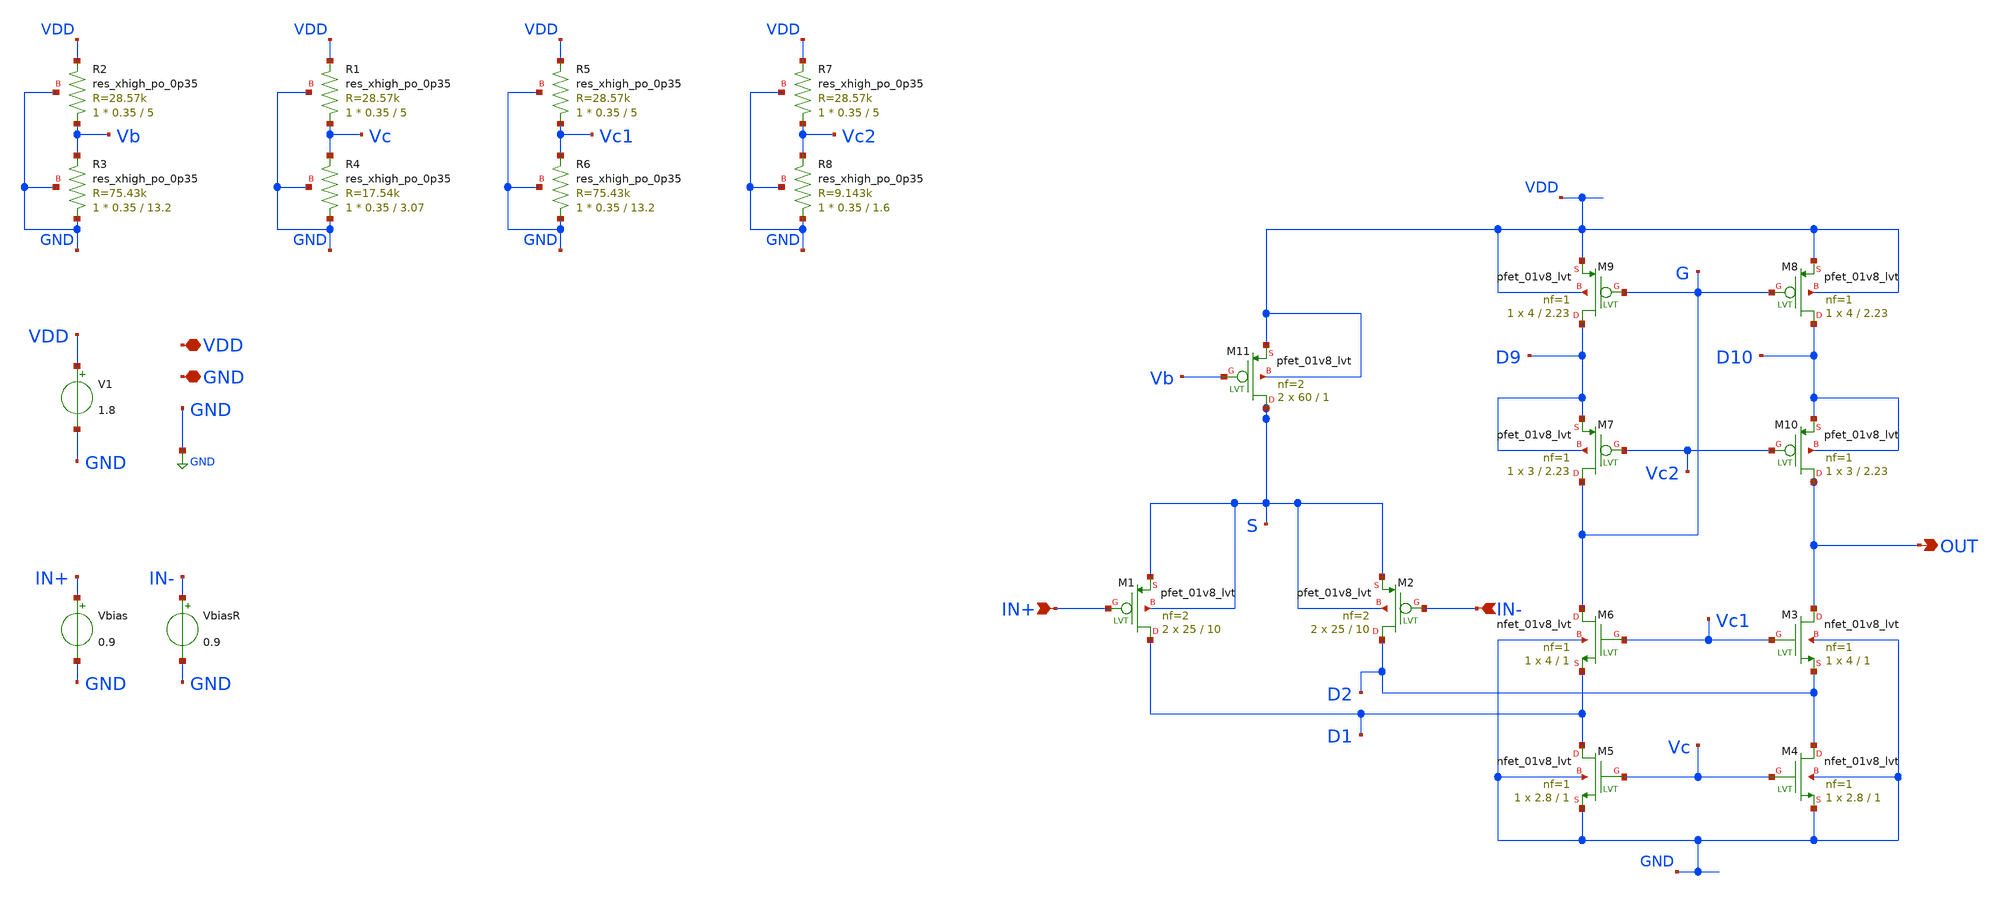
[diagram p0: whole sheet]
** sch_path: xschem/OTA_FoldedCascode1_MC.sch
**.subckt OTA_FoldedCascode1_MC VDD GND IN+ IN- OUT
*.iopin VDD
*.iopin GND
*.ipin IN+
*.ipin IN-
*.opin OUT
V1 VDD GND 1.8
Vbias IN+ GND 0.9
VbiasR IN- GND 0.9
XM11 S Vb VDD VDD sky130_fd_pr__pfet_01v8_lvt L=1 W=60 nf=2 ad='int((nf+1)/2) * W/nf * 0.29' as='int((nf+2)/2) * W/nf * 0.29'
+ pd='2*int((nf+1)/2) * (W/nf + 0.29)' ps='2*int((nf+2)/2) * (W/nf + 0.29)' nrd='0.29 / W' nrs='0.29 / W'
+ sa=0 sb=0 sd=0 mult=2 m=2
XM1 D1 IN+ S S sky130_fd_pr__pfet_01v8_lvt L=10 W=25 nf=2 ad='int((nf+1)/2) * W/nf * 0.29' as='int((nf+2)/2) * W/nf * 0.29'
+ pd='2*int((nf+1)/2) * (W/nf + 0.29)' ps='2*int((nf+2)/2) * (W/nf + 0.29)' nrd='0.29 / W' nrs='0.29 / W'
+ sa=0 sb=0 sd=0 mult=2 m=2
XM2 D2 IN- S S sky130_fd_pr__pfet_01v8_lvt L=10 W=25 nf=2 ad='int((nf+1)/2) * W/nf * 0.29' as='int((nf+2)/2) * W/nf * 0.29'
+ pd='2*int((nf+1)/2) * (W/nf + 0.29)' ps='2*int((nf+2)/2) * (W/nf + 0.29)' nrd='0.29 / W' nrs='0.29 / W'
+ sa=0 sb=0 sd=0 mult=2 m=2
XM3 OUT Vc1 D2 GND sky130_fd_pr__nfet_01v8_lvt L=1 W=4 nf=1 ad='int((nf+1)/2) * W/nf * 0.29' as='int((nf+2)/2) * W/nf * 0.29'
+ pd='2*int((nf+1)/2) * (W/nf + 0.29)' ps='2*int((nf+2)/2) * (W/nf + 0.29)' nrd='0.29 / W' nrs='0.29 / W'
+ sa=0 sb=0 sd=0 mult=1 m=1
XM4 D2 Vc GND GND sky130_fd_pr__nfet_01v8_lvt L=1 W=2.8 nf=1 ad='int((nf+1)/2) * W/nf * 0.29' as='int((nf+2)/2) * W/nf * 0.29'
+ pd='2*int((nf+1)/2) * (W/nf + 0.29)' ps='2*int((nf+2)/2) * (W/nf + 0.29)' nrd='0.29 / W' nrs='0.29 / W'
+ sa=0 sb=0 sd=0 mult=1 m=1
XM5 D1 Vc GND GND sky130_fd_pr__nfet_01v8_lvt L=1 W=2.8 nf=1 ad='int((nf+1)/2) * W/nf * 0.29' as='int((nf+2)/2) * W/nf * 0.29'
+ pd='2*int((nf+1)/2) * (W/nf + 0.29)' ps='2*int((nf+2)/2) * (W/nf + 0.29)' nrd='0.29 / W' nrs='0.29 / W'
+ sa=0 sb=0 sd=0 mult=1 m=1
XM6 G Vc1 D1 GND sky130_fd_pr__nfet_01v8_lvt L=1 W=4 nf=1 ad='int((nf+1)/2) * W/nf * 0.29' as='int((nf+2)/2) * W/nf * 0.29'
+ pd='2*int((nf+1)/2) * (W/nf + 0.29)' ps='2*int((nf+2)/2) * (W/nf + 0.29)' nrd='0.29 / W' nrs='0.29 / W'
+ sa=0 sb=0 sd=0 mult=1 m=1
XM7 G Vc2 D9 D9 sky130_fd_pr__pfet_01v8_lvt L=2.23 W=3 nf=1 ad='int((nf+1)/2) * W/nf * 0.29' as='int((nf+2)/2) * W/nf * 0.29'
+ pd='2*int((nf+1)/2) * (W/nf + 0.29)' ps='2*int((nf+2)/2) * (W/nf + 0.29)' nrd='0.29 / W' nrs='0.29 / W'
+ sa=0 sb=0 sd=0 mult=1 m=1
XM9 D9 G VDD VDD sky130_fd_pr__pfet_01v8_lvt L=2.23 W=4 nf=1 ad='int((nf+1)/2) * W/nf * 0.29' as='int((nf+2)/2) * W/nf * 0.29'
+ pd='2*int((nf+1)/2) * (W/nf + 0.29)' ps='2*int((nf+2)/2) * (W/nf + 0.29)' nrd='0.29 / W' nrs='0.29 / W'
+ sa=0 sb=0 sd=0 mult=1 m=1
XM8 D10 G VDD VDD sky130_fd_pr__pfet_01v8_lvt L=2.23 W=4 nf=1 ad='int((nf+1)/2) * W/nf * 0.29' as='int((nf+2)/2) * W/nf * 0.29'
+ pd='2*int((nf+1)/2) * (W/nf + 0.29)' ps='2*int((nf+2)/2) * (W/nf + 0.29)' nrd='0.29 / W' nrs='0.29 / W'
+ sa=0 sb=0 sd=0 mult=1 m=1
XM10 OUT Vc2 D10 D10 sky130_fd_pr__pfet_01v8_lvt L=2.23 W=3 nf=1 ad='int((nf+1)/2) * W/nf * 0.29' as='int((nf+2)/2) * W/nf * 0.29'
+ pd='2*int((nf+1)/2) * (W/nf + 0.29)' ps='2*int((nf+2)/2) * (W/nf + 0.29)' nrd='0.29 / W' nrs='0.29 / W'
+ sa=0 sb=0 sd=0 mult=1 m=1
XR2 Vb VDD GND sky130_fd_pr__res_xhigh_po_0p35 L=5 mult=1 m=1
XR3 GND Vb GND sky130_fd_pr__res_xhigh_po_0p35 L=13.2 mult=1 m=1
XR1 Vc VDD GND sky130_fd_pr__res_xhigh_po_0p35 L=5 mult=1 m=1
XR4 GND Vc GND sky130_fd_pr__res_xhigh_po_0p35 L=3.07 mult=1 m=1
XR5 Vc1 VDD GND sky130_fd_pr__res_xhigh_po_0p35 L=5 mult=1 m=1
XR6 GND Vc1 GND sky130_fd_pr__res_xhigh_po_0p35 L=13.2 mult=1 m=1
XR7 Vc2 VDD GND sky130_fd_pr__res_xhigh_po_0p35 L=5 mult=1 m=1
XR8 GND Vc2 GND sky130_fd_pr__res_xhigh_po_0p35 L=1.6 mult=1 m=1
**** begin user architecture code


.options savecurrents
.control
    destroy all

    * Usiamo 20 run per testare la stabilità
    let mc_runs = 20
    let run_idx = 0

    * Inizializziamo i vettori nel plot 'const'
    let const.gain_out = unitvec(20)
    let const.run_num = unitvec(20)

    * --- INIZIO LOOP ---
    repeat 20

        * Sweep DC molto largo per non perdere mai il picco
        dc Vbias 0.80 1.00 0.001

        * Definiamo il vettore della derivata nel plot corrente
        let d_out = deriv(v(out))

        * Troviamo il massimo usando una sintassi più tollerante
        let g_peak = vecmax(d_out)

        * Salvataggio forzato indicando esplicitamente il plot 'const'
        let const.gain_out[run_idx] = g_peak
        let const.run_num[run_idx] = run_idx

        echo

        let run_idx = run_idx + 1
        reset
    end
    * --- FINE LOOP ---

    * Torniamo al plot globale per evitare errori di 'no such vector'
    setplot const

    echo
    * Stampiamo i valori grezzi (se avg dà errore, vedremo almeno la lista)
    print gain_out

    * Il grafico DEVE usare 'vs' per allineare i 20 punti
    plot gain_out vs run_num title 'Guadagno per Run'
.endc
.end


.lib $::SKYWATER_MODELS/sky130.lib.spice tt
**** end user architecture code
**.ends
.GLOBAL GND
.end
